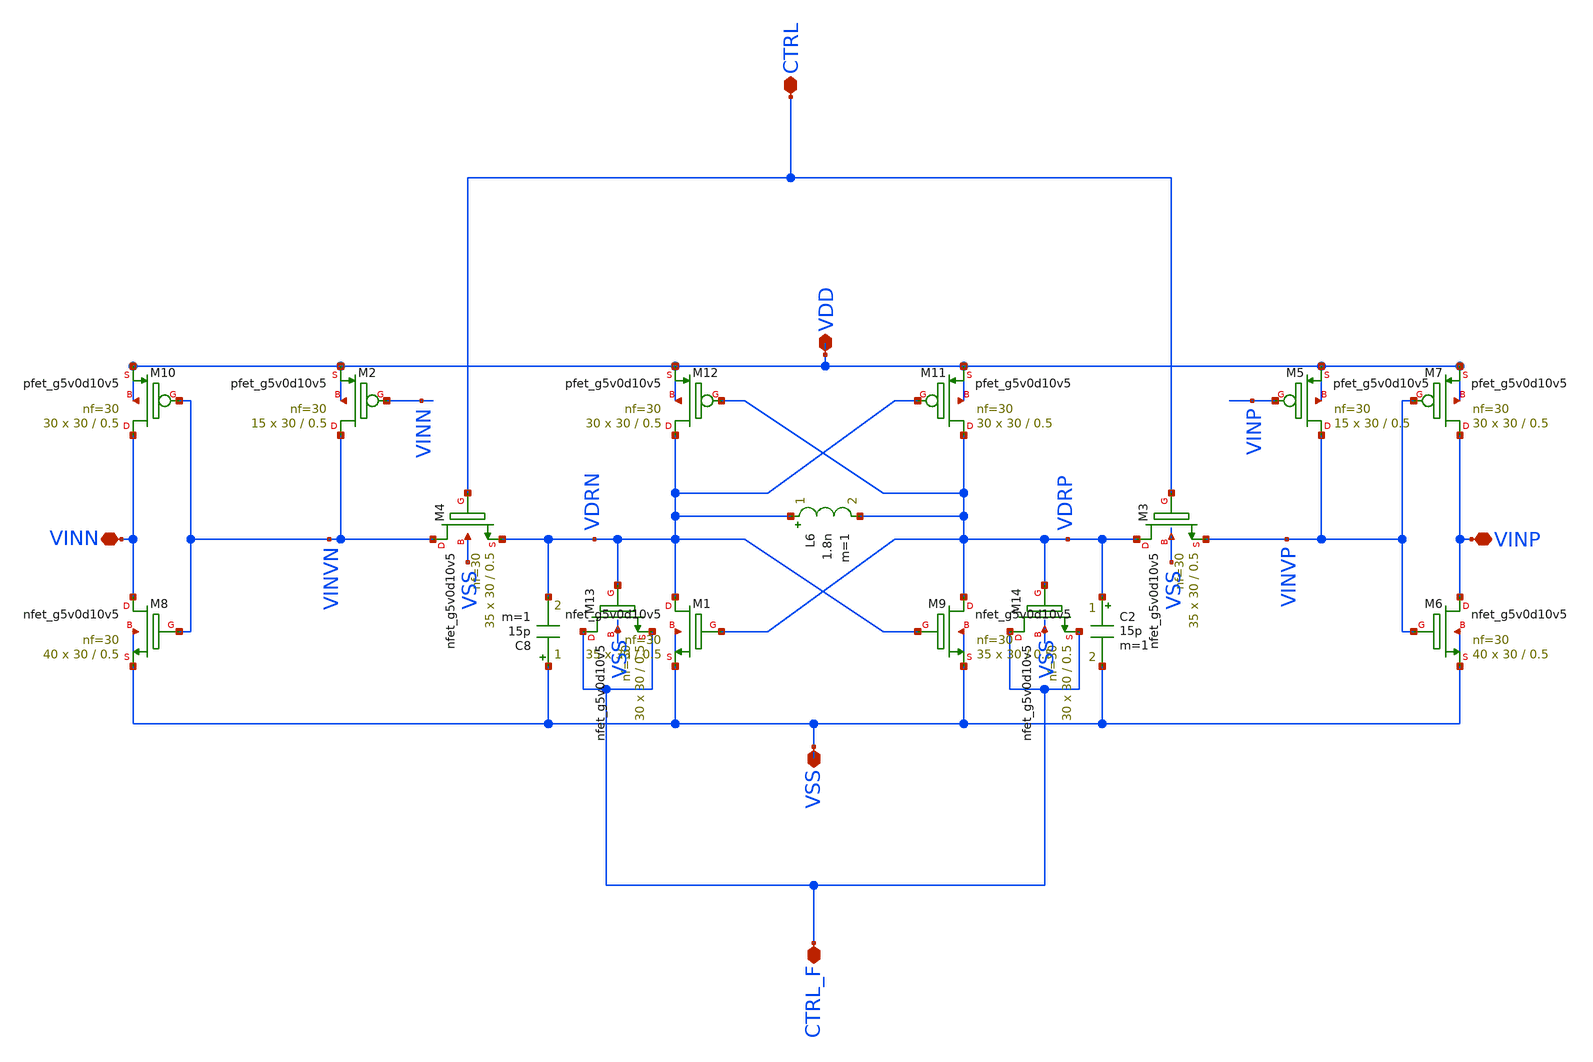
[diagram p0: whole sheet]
** sch_path: xschem/Cmos_DIV_TG_KPER.sch
**.subckt Cmos_DIV_TG_KPER VDD VSS VINN VINP CTRL CTRL_F
*.iopin VDD
*.iopin VSS
*.iopin VINN
*.iopin VINP
*.iopin CTRL
*.iopin CTRL_F
XM9 VDRP VDRN VSS VSS sky130_fd_pr__nfet_g5v0d10v5 L=0.5 W=30 nf=30 ad='int((nf+1)/2) * W/nf * 0.29'
+ as='int((nf+2)/2) * W/nf * 0.29' pd='2*int((nf+1)/2) * (W/nf + 0.29)' ps='2*int((nf+2)/2) * (W/nf + 0.29)'
+ nrd='0.29 / W' nrs='0.29 / W' sa=0 sb=0 sd=0 mult=35 m=35
XM1 VDRN VDRP VSS VSS sky130_fd_pr__nfet_g5v0d10v5 L=0.5 W=30 nf=30 ad='int((nf+1)/2) * W/nf * 0.29'
+ as='int((nf+2)/2) * W/nf * 0.29' pd='2*int((nf+1)/2) * (W/nf + 0.29)' ps='2*int((nf+2)/2) * (W/nf + 0.29)'
+ nrd='0.29 / W' nrs='0.29 / W' sa=0 sb=0 sd=0 mult=35 m=35
L6 VDRN VDRP 1.8n m=1
C2 VDRP VSS 15p m=1
C8 VSS VDRN 15p m=1
XM4 VINVN CTRL VDRN VSS sky130_fd_pr__nfet_g5v0d10v5 L=0.5 W=30 nf=30 ad='int((nf+1)/2) * W/nf * 0.29'
+ as='int((nf+2)/2) * W/nf * 0.29' pd='2*int((nf+1)/2) * (W/nf + 0.29)' ps='2*int((nf+2)/2) * (W/nf + 0.29)'
+ nrd='0.29 / W' nrs='0.29 / W' sa=0 sb=0 sd=0 mult=35 m=35
XM6 VINP VINVP VSS VSS sky130_fd_pr__nfet_g5v0d10v5 L=0.5 W=30 nf=30 ad='int((nf+1)/2) * W/nf * 0.29'
+ as='int((nf+2)/2) * W/nf * 0.29' pd='2*int((nf+1)/2) * (W/nf + 0.29)' ps='2*int((nf+2)/2) * (W/nf + 0.29)'
+ nrd='0.29 / W' nrs='0.29 / W' sa=0 sb=0 sd=0 mult=40 m=40
XM7 VINP VINVP VDD VDD sky130_fd_pr__pfet_g5v0d10v5 L=0.5 W=30 nf=30 ad='int((nf+1)/2) * W/nf * 0.29'
+ as='int((nf+2)/2) * W/nf * 0.29' pd='2*int((nf+1)/2) * (W/nf + 0.29)' ps='2*int((nf+2)/2) * (W/nf + 0.29)'
+ nrd='0.29 / W' nrs='0.29 / W' sa=0 sb=0 sd=0 mult=30 m=30
XM8 VINN VINVN VSS VSS sky130_fd_pr__nfet_g5v0d10v5 L=0.5 W=30 nf=30 ad='int((nf+1)/2) * W/nf * 0.29'
+ as='int((nf+2)/2) * W/nf * 0.29' pd='2*int((nf+1)/2) * (W/nf + 0.29)' ps='2*int((nf+2)/2) * (W/nf + 0.29)'
+ nrd='0.29 / W' nrs='0.29 / W' sa=0 sb=0 sd=0 mult=40 m=40
XM10 VINN VINVN VDD VDD sky130_fd_pr__pfet_g5v0d10v5 L=0.5 W=30 nf=30 ad='int((nf+1)/2) * W/nf * 0.29'
+ as='int((nf+2)/2) * W/nf * 0.29' pd='2*int((nf+1)/2) * (W/nf + 0.29)' ps='2*int((nf+2)/2) * (W/nf + 0.29)'
+ nrd='0.29 / W' nrs='0.29 / W' sa=0 sb=0 sd=0 mult=30 m=30
XM13 CTRL_F VDRN CTRL_F VSS sky130_fd_pr__nfet_g5v0d10v5 L=0.5 W=30 nf=30 ad='int((nf+1)/2) * W/nf * 0.29'
+ as='int((nf+2)/2) * W/nf * 0.29' pd='2*int((nf+1)/2) * (W/nf + 0.29)' ps='2*int((nf+2)/2) * (W/nf + 0.29)'
+ nrd='0.29 / W' nrs='0.29 / W' sa=0 sb=0 sd=0 mult=30 m=30
XM14 CTRL_F VDRP CTRL_F VSS sky130_fd_pr__nfet_g5v0d10v5 L=0.5 W=30 nf=30 ad='int((nf+1)/2) * W/nf * 0.29'
+ as='int((nf+2)/2) * W/nf * 0.29' pd='2*int((nf+1)/2) * (W/nf + 0.29)' ps='2*int((nf+2)/2) * (W/nf + 0.29)'
+ nrd='0.29 / W' nrs='0.29 / W' sa=0 sb=0 sd=0 mult=30 m=30
XM11 VDRP VDRN VDD VDD sky130_fd_pr__pfet_g5v0d10v5 L=0.5 W=30 nf=30 ad='int((nf+1)/2) * W/nf * 0.29'
+ as='int((nf+2)/2) * W/nf * 0.29' pd='2*int((nf+1)/2) * (W/nf + 0.29)' ps='2*int((nf+2)/2) * (W/nf + 0.29)'
+ nrd='0.29 / W' nrs='0.29 / W' sa=0 sb=0 sd=0 mult=30 m=30
XM12 VDRN VDRP VDD VDD sky130_fd_pr__pfet_g5v0d10v5 L=0.5 W=30 nf=30 ad='int((nf+1)/2) * W/nf * 0.29'
+ as='int((nf+2)/2) * W/nf * 0.29' pd='2*int((nf+1)/2) * (W/nf + 0.29)' ps='2*int((nf+2)/2) * (W/nf + 0.29)'
+ nrd='0.29 / W' nrs='0.29 / W' sa=0 sb=0 sd=0 mult=30 m=30
XM3 VDRP CTRL VINVP VSS sky130_fd_pr__nfet_g5v0d10v5 L=0.5 W=30 nf=30 ad='int((nf+1)/2) * W/nf * 0.29'
+ as='int((nf+2)/2) * W/nf * 0.29' pd='2*int((nf+1)/2) * (W/nf + 0.29)' ps='2*int((nf+2)/2) * (W/nf + 0.29)'
+ nrd='0.29 / W' nrs='0.29 / W' sa=0 sb=0 sd=0 mult=35 m=35
XM2 VINVN VINN VDD VDD sky130_fd_pr__pfet_g5v0d10v5 L=0.5 W=30 nf=30 ad='int((nf+1)/2) * W/nf * 0.29'
+ as='int((nf+2)/2) * W/nf * 0.29' pd='2*int((nf+1)/2) * (W/nf + 0.29)' ps='2*int((nf+2)/2) * (W/nf + 0.29)'
+ nrd='0.29 / W' nrs='0.29 / W' sa=0 sb=0 sd=0 mult=15 m=15
XM5 VINVP VINP VDD VDD sky130_fd_pr__pfet_g5v0d10v5 L=0.5 W=30 nf=30 ad='int((nf+1)/2) * W/nf * 0.29'
+ as='int((nf+2)/2) * W/nf * 0.29' pd='2*int((nf+1)/2) * (W/nf + 0.29)' ps='2*int((nf+2)/2) * (W/nf + 0.29)'
+ nrd='0.29 / W' nrs='0.29 / W' sa=0 sb=0 sd=0 mult=15 m=15
**.ends
.end
